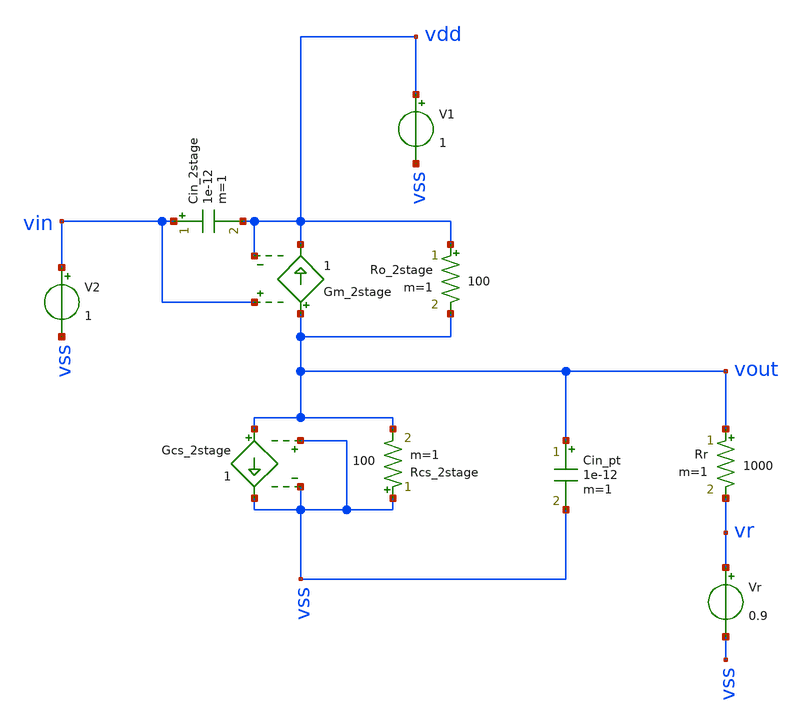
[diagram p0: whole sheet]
** sch_path: test/Tesis_notebooks/xschem/ota_2stage_rout_v2.sch
**.subckt ota_2stage_rout_v2
Vr vr vss 0.9
Rr vout vr 1000 m=1
Ro_2stage vdd vout 100 m=1
Gm_2stage vout vdd vin vdd 1
V1 vdd vss 1
Cin_2stage vin vdd 1e-12 m=1
V2 vin vss 1
Gcs_2stage vout vss vss vss 1
Rcs_2stage vss vout 100 m=1
Cin_pt vout vss 1e-12 m=1
**.ends
.end
